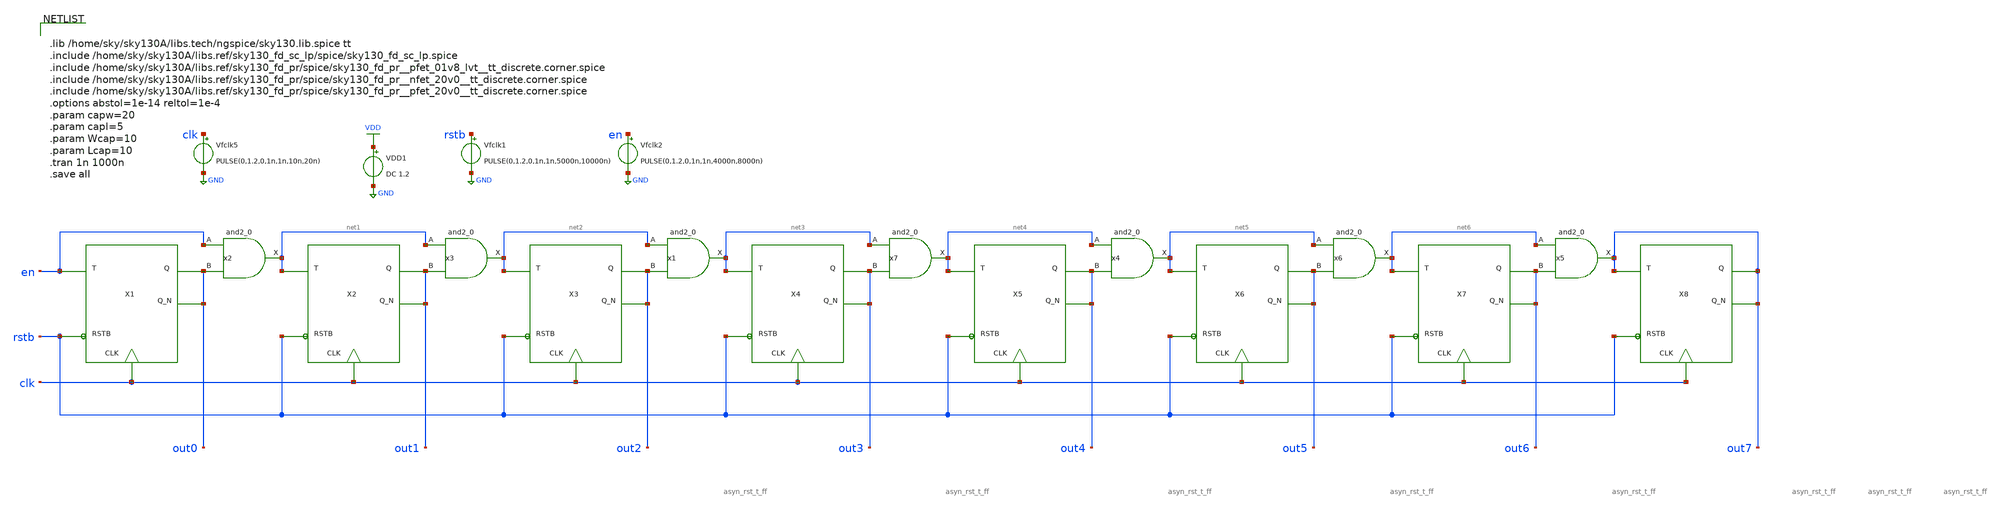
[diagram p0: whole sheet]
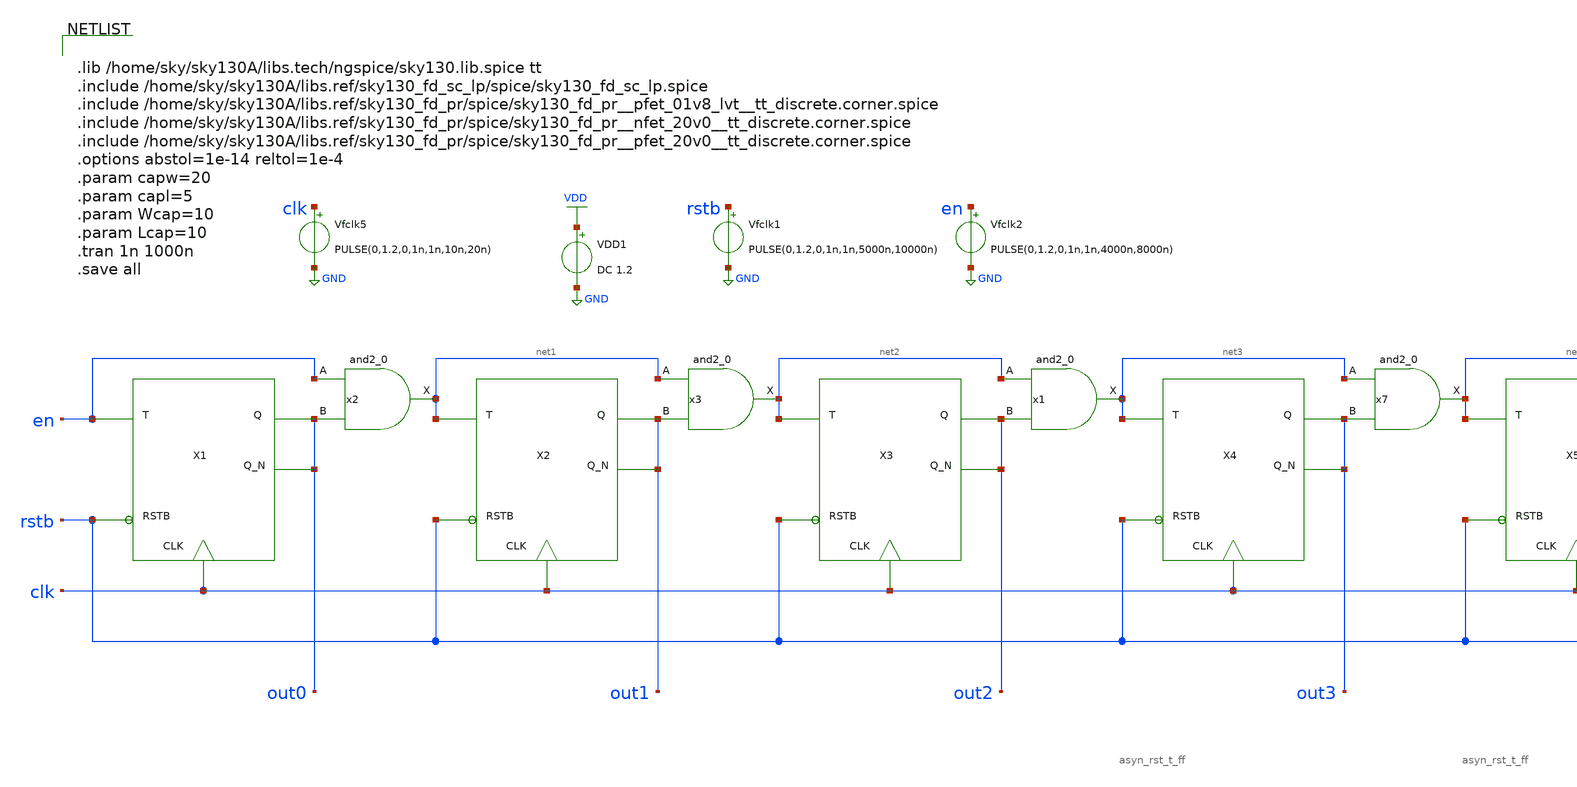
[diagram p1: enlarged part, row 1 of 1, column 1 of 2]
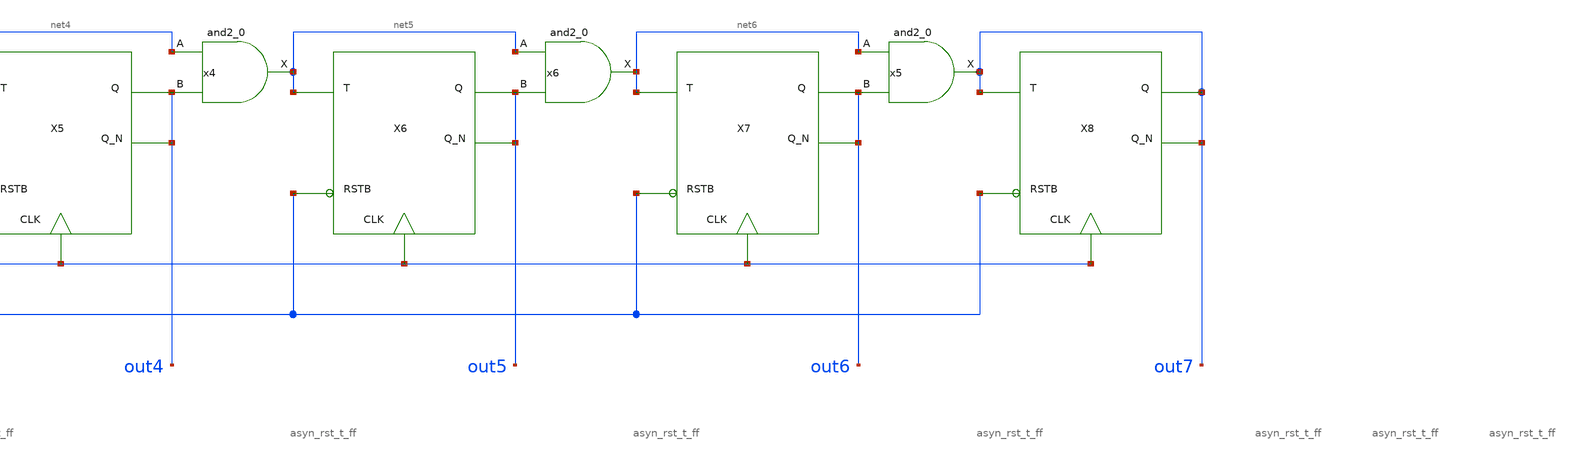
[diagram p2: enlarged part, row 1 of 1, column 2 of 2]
** sch_path: xschem/tryandtest/final/gray_counter.sch
**.subckt gray_counter
X1 en out0 clk rstb out0 asyn_rst_t_ff
X2 net1 out1 clk rstb out1 asyn_rst_t_ff
x2 en out0 gnd gnd vdd vdd net1 sky130_fd_sc_lp__and2_0
X3 net2 out2 clk rstb out2 asyn_rst_t_ff
X4 net3 out3 clk rstb out3 asyn_rst_t_ff
x1 net2 out2 gnd gnd vdd vdd net3 sky130_fd_sc_lp__and2_0
x3 net1 out1 gnd gnd vdd vdd net2 sky130_fd_sc_lp__and2_0
X5 net4 out4 clk rstb out4 asyn_rst_t_ff
X6 net5 out5 clk rstb out5 asyn_rst_t_ff
x4 net4 out4 gnd gnd vdd vdd net5 sky130_fd_sc_lp__and2_0
X7 net6 out6 clk rstb out6 asyn_rst_t_ff
X8 out7 out7 clk rstb out7 asyn_rst_t_ff
x5 net6 out6 gnd gnd vdd vdd out7 sky130_fd_sc_lp__and2_0
x6 net5 out5 gnd gnd vdd vdd net6 sky130_fd_sc_lp__and2_0
x7 net3 out3 gnd gnd vdd vdd net4 sky130_fd_sc_lp__and2_0
VDD1 VDD GND DC 1.2
Vfclk5 clk GND PULSE(0,1.2,0,1n,1n,10n,20n)
Vfclk1 rstb GND PULSE(0,1.2,0,1n,1n,5000n,10000n)
Vfclk2 en GND PULSE(0,1.2,0,1n,1n,4000n,8000n)
**** begin user architecture code


.lib /home/sky/sky130A/libs.tech/ngspice/sky130.lib.spice tt
.include /home/sky/sky130A/libs.ref/sky130_fd_sc_lp/spice/sky130_fd_sc_lp.spice
.include /home/sky/sky130A/libs.ref/sky130_fd_pr/spice/sky130_fd_pr__pfet_01v8_lvt__tt_discrete.corner.spice
.include /home/sky/sky130A/libs.ref/sky130_fd_pr/spice/sky130_fd_pr__nfet_20v0__tt_discrete.corner.spice
.include /home/sky/sky130A/libs.ref/sky130_fd_pr/spice/sky130_fd_pr__pfet_20v0__tt_discrete.corner.spice
.options abstol=1e-14 reltol=1e-4
.param capw=20
.param capl=5
.param Wcap=10
.param Lcap=10
.tran 1n 1000n
.save all


**** end user architecture code
**.ends

* expanding   symbol:  T_flip_flop/asyn_rst_t_ff.sym # of pins=5
** sym_path: xschem/T_flip_flop/asyn_rst_t_ff.sym
** sch_path: xschem/T_flip_flop/asyn_rst_t_ff.sch
.subckt asyn_rst_t_ff T Q CLK RSTB Q_N
*.ipin T
*.ipin CLK
*.opin Q
*.ipin RSTB
*.opin Q_N
x3 T Q GND GND VDD VDD net1 sky130_fd_sc_lp__xor2_1
x2 Q GND GND VDD VDD Q_N sky130_fd_sc_lp__inv_1
x1 CLK net1 RSTB GND GND VDD VDD Q sky130_fd_sc_lp__dfrtp_1
.ends

.GLOBAL GND
.GLOBAL VDD
.end
